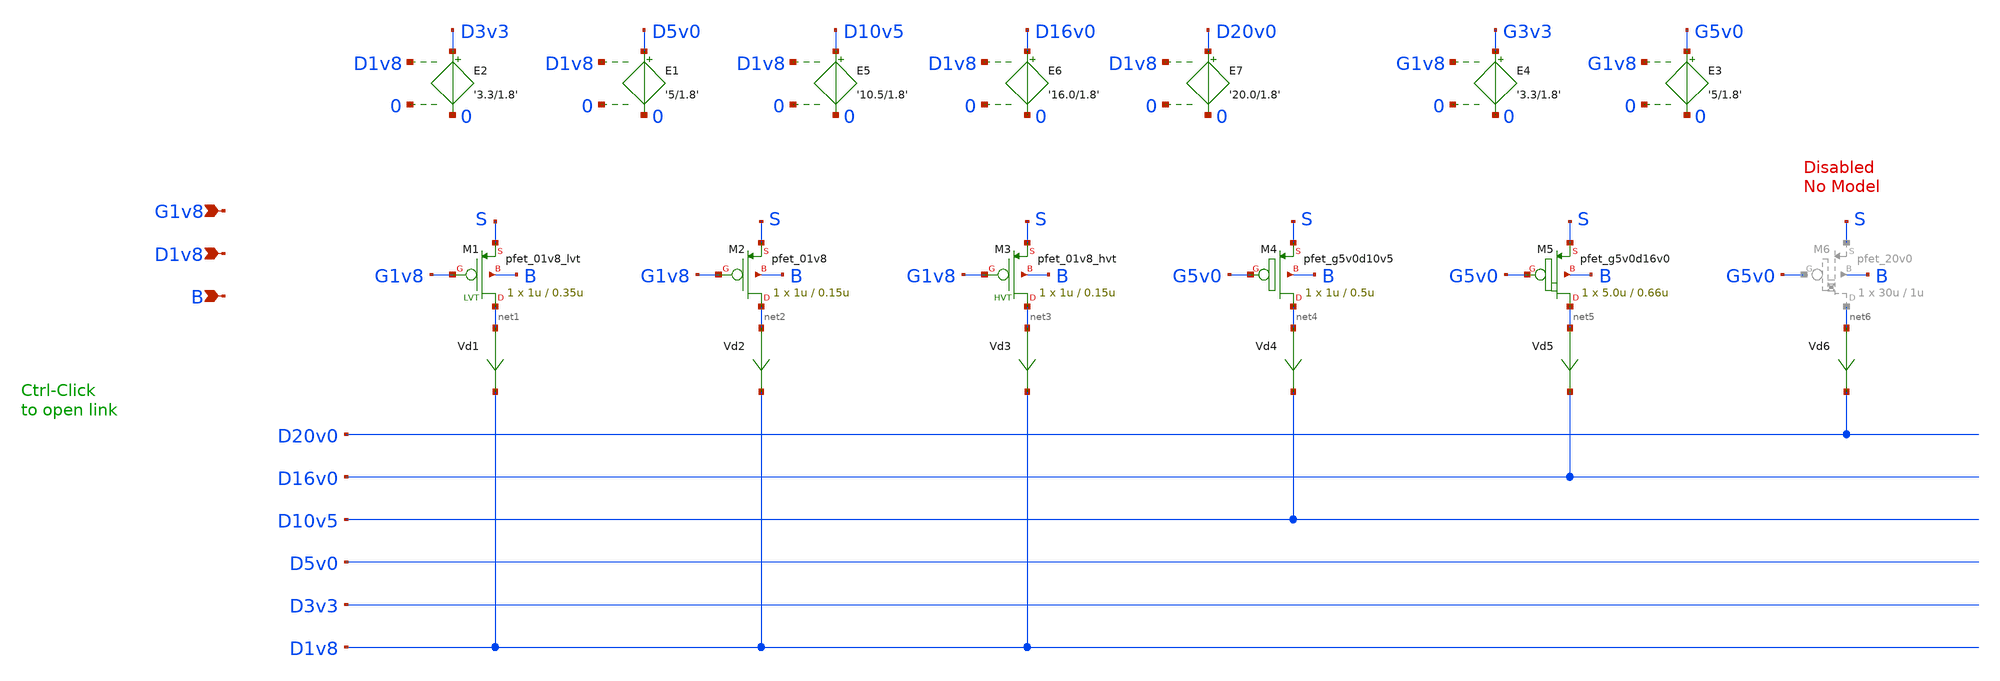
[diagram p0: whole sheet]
** sch_path: sky130_tests_X/test_pmos2.sch
* Copyright 2020 Stefan Frederik Schippers
* Licensed under the Apache License, Version 2.0 (the "License");
* you may not use this file except in compliance with the License.
* You may obtain a copy of the License at
* https://www.apache.org/licenses/LICENSE-2.0
* Unless required by applicable law or agreed to in writing, software
* distributed under the License is distributed on an "AS IS" BASIS,
* WITHOUT WARRANTIES OR CONDITIONS OF ANY KIND, either express or implied.
* See the License for the specific language governing permissions and
* limitations under the License.
**.subckt test_pmos2 G1v8 D1v8 B
*.ipin G1v8
*.ipin D1v8
*.ipin B
Vd1 net1 D1v8 0
.save i(vd1)
Vd2 net2 D1v8 0
.save i(vd2)
E1 D5v0 0 D1v8 0 '5/1.8'
E2 D3v3 0 D1v8 0 '3.3/1.8'
E3 G5v0 0 G1v8 0 '5/1.8'
E4 G3v3 0 G1v8 0 '3.3/1.8'
E5 D10v5 0 D1v8 0 '10.5/1.8'
Vd3 net3 D1v8 0
.save i(vd3)
XM3 net3 G1v8 S B sky130_fd_pr__pfet_01v8_hvt w=1u l=0.15u ad=[sky130_fet_ad_cb 1u ]
+ pd=[sky130_fet_pd_cb 1u ] as=[sky130_fet_ad_cb 1u ] ps=[sky130_fet_pd_cb 1u ] nrd=[sky130_fet_nrd_cb 1u ]
+ nrs=[sky130_fet_nrd_cb 1u ] sa=0 sb=0 sd=0 nf=1 mult=1 m=1
Vd4 net4 D10v5 0
.save i(vd4)
XM4 net4 G5v0 S B sky130_fd_pr__pfet_g5v0d10v5 w=1u l=0.5u ad=[sky130_fet_ad_cb 1u ]
+ pd=[sky130_fet_pd_cb 1u ] as=[sky130_fet_ad_cb 1u ] ps=[sky130_fet_pd_cb 1u ] nrd=[sky130_fet_nrd_cb 1u ]
+ nrs=[sky130_fet_nrd_cb 1u ] sa=0 sb=0 sd=0 nf=1 mult=1 m=1
XM1 net1 G1v8 S B sky130_fd_pr__pfet_01v8_lvt w=1u l=0.35u ad=[sky130_fet_ad_cb 1u ]
+ pd=[sky130_fet_pd_cb 1u ] as=[sky130_fet_ad_cb 1u ] ps=[sky130_fet_pd_cb 1u ] nrd=[sky130_fet_nrd_cb 1u ]
+ nrs=[sky130_fet_nrd_cb 1u ] sa=0 sb=0 sd=0 nf=1 mult=1 m=1
XM2 net2 G1v8 S B sky130_fd_pr__pfet_01v8 w=1u l=0.15u ad=[sky130_fet_ad_cb 1u ]
+ pd=[sky130_fet_pd_cb 1u ] as=[sky130_fet_ad_cb 1u ] ps=[sky130_fet_pd_cb 1u ] nrd=[sky130_fet_nrd_cb 1u ]
+ nrs=[sky130_fet_nrd_cb 1u ] sa=0 sb=0 sd=0 nf=1 mult=1 m=1
Vd5 net5 D16v0 0
.save i(vd5)
XM5 net5 G5v0 S B sky130_fd_pr__pfet_g5v0d16v0 w=5.0u l=0.66u ad=[sky130_fet_ad_cb 5.0u ]
+ pd=[sky130_fet_pd_cb 5.0u ] as=[sky130_fet_ad_cb 5.0u ] ps=[sky130_fet_pd_cb 5.0u ] nrd=[sky130_fet_nrd_cb 5.0u ]
+ nrs=[sky130_fet_nrd_cb 5.0u ] sa=0 sb=0 sd=0 nf=1 mult=1 m=1
E6 D16v0 0 D1v8 0 '16.0/1.8'
E7 D20v0 0 D1v8 0 '20.0/1.8'
Vd6 net6 D20v0 0
.save i(vd6)
**** begin user architecture code


vg G1v8 0 0
vs s 0 0
vd D1v8 0 0
vb b 0 0
.control
dc vd 0 -1.8 -0.01 vg 0 -1.8 -0.2
plot all.vd1#branch vs D1v8
plot all.vd2#branch vs D1v8
plot all.vd3#branch vs D1v8
plot all.vd4#branch vs D10v5
plot all.vd5#branch vs D16v0

.endc



**** end user architecture code
**.ends
.end
